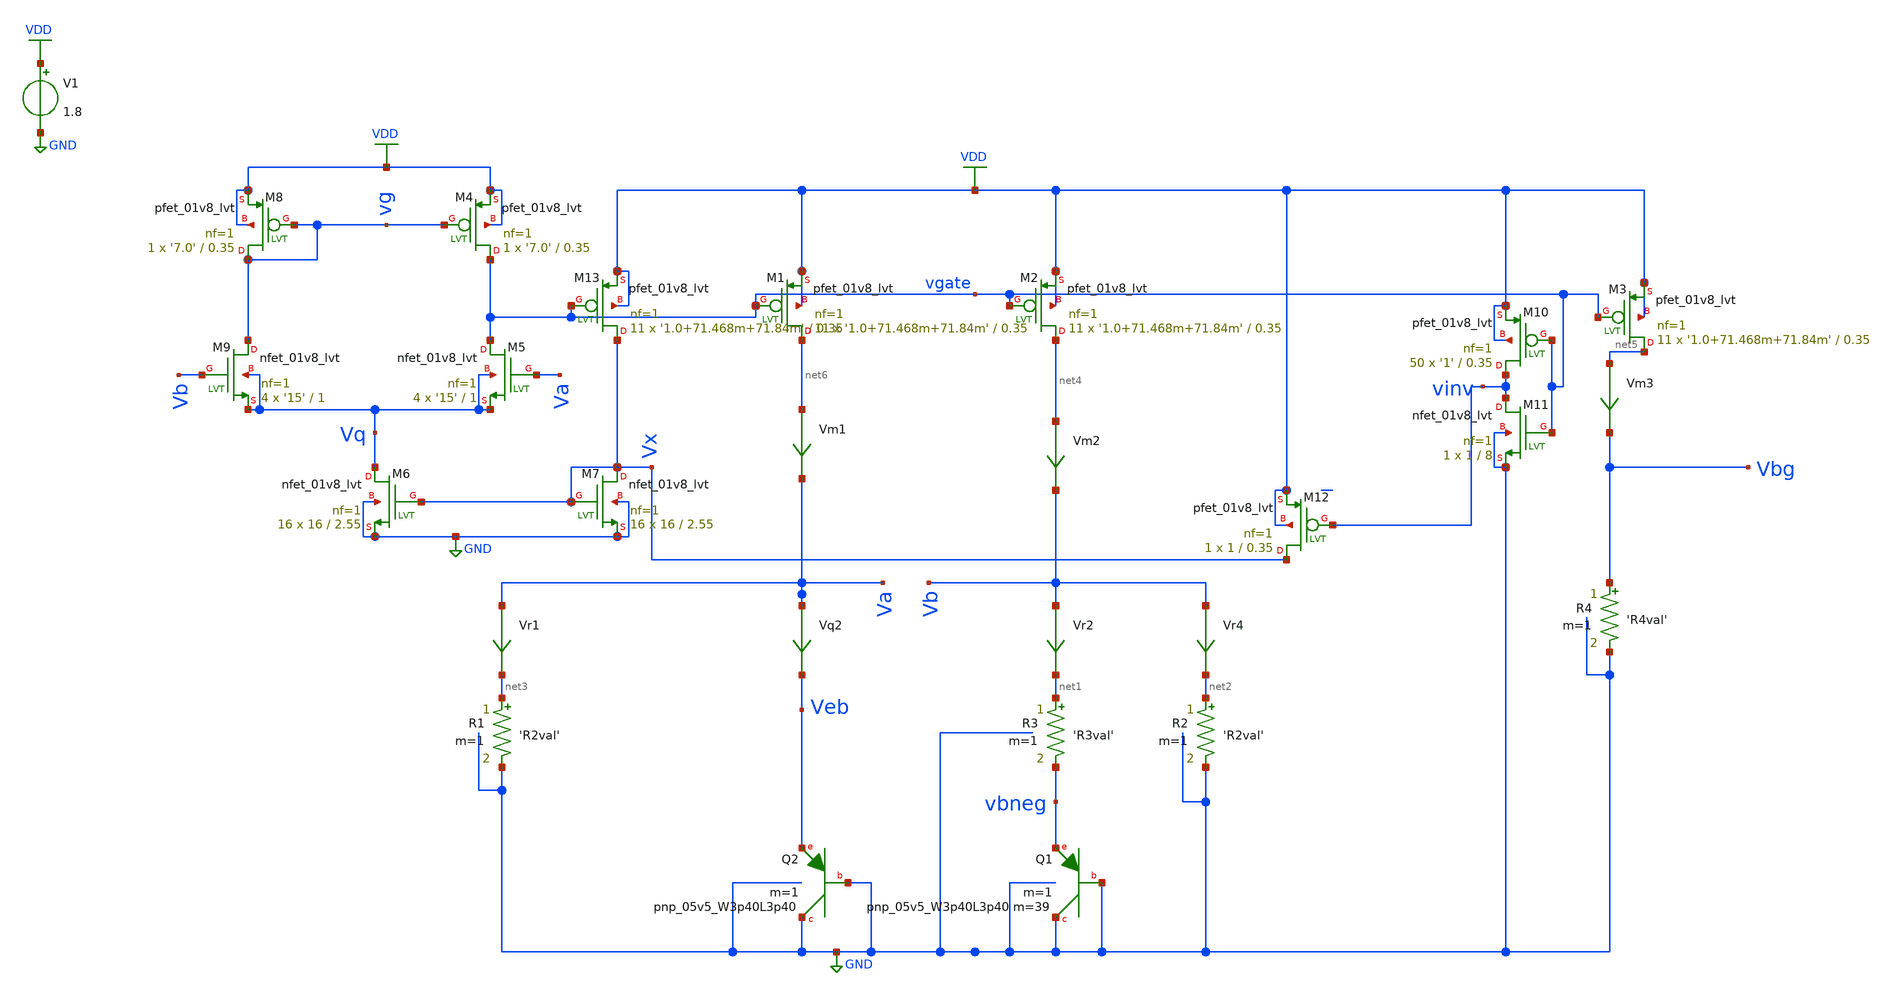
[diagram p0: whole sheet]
** sch_path: schematics/tsmc_bandgap_real_non_pdk_res.sch
**.subckt tsmc_bandgap_real_non_pdk_res
XQ2 GND GND Veb sky130_fd_pr__pnp_05v5_W3p40L3p40 m=1
V1 VDD GND 1.8
Vr4 Vb net2 0
.save i(vr4)
Vr2 Vb net1 0
.save i(vr2)
Vm1 net6 Va 0
.save i(vm1)
Vm2 net4 Vb 0
.save i(vm2)
Vm3 net5 Vbg 0
.save i(vm3)
Vr1 Va net3 0
.save i(vr1)
Vq2 Va Veb 0
.save i(vq2)
XQ1 GND GND vbneg sky130_fd_pr__pnp_05v5_W3p40L3p40 m=39 m=1
R3 net1 vbneg 'R3val' m=1
R4 Vbg GND 'R4val' m=1
R1 net3 GND 'R2val' m=1
R2 net2 GND 'R2val' m=1
XM4 vgate vg VDD VDD sky130_fd_pr__pfet_01v8_lvt L=0.35 W='7.0' nf=1 ad='int((nf+1)/2) * W/nf * 0.29'
+ as='int((nf+2)/2) * W/nf * 0.29' pd='2*int((nf+1)/2) * (W/nf + 0.29)' ps='2*int((nf+2)/2) * (W/nf + 0.29)'
+ nrd='0.29 / W' nrs='0.29 / W' sa=0 sb=0 sd=0 mult=1 m=1
XM5 vgate Va Vq Vq sky130_fd_pr__nfet_01v8_lvt L=1 W='15' nf=1 ad='int((nf+1)/2) * W/nf * 0.29' as='int((nf+2)/2) * W/nf * 0.29'
+ pd='2*int((nf+1)/2) * (W/nf + 0.29)' ps='2*int((nf+2)/2) * (W/nf + 0.29)' nrd='0.29 / W' nrs='0.29 / W'
+ sa=0 sb=0 sd=0 mult=4 m=4
XM6 Vq Vx GND GND sky130_fd_pr__nfet_01v8_lvt L=2.55 W=16 nf=1 ad='int((nf+1)/2) * W/nf * 0.29' as='int((nf+2)/2) * W/nf * 0.29'
+ pd='2*int((nf+1)/2) * (W/nf + 0.29)' ps='2*int((nf+2)/2) * (W/nf + 0.29)' nrd='0.29 / W' nrs='0.29 / W'
+ sa=0 sb=0 sd=0 mult=16 m=16
XM8 vg vg VDD VDD sky130_fd_pr__pfet_01v8_lvt L=0.35 W='7.0' nf=1 ad='int((nf+1)/2) * W/nf * 0.29' as='int((nf+2)/2) * W/nf * 0.29'
+ pd='2*int((nf+1)/2) * (W/nf + 0.29)' ps='2*int((nf+2)/2) * (W/nf + 0.29)' nrd='0.29 / W' nrs='0.29 / W'
+ sa=0 sb=0 sd=0 mult=1 m=1
XM9 vg Vb Vq Vq sky130_fd_pr__nfet_01v8_lvt L=1 W='15' nf=1 ad='int((nf+1)/2) * W/nf * 0.29' as='int((nf+2)/2) * W/nf * 0.29'
+ pd='2*int((nf+1)/2) * (W/nf + 0.29)' ps='2*int((nf+2)/2) * (W/nf + 0.29)' nrd='0.29 / W' nrs='0.29 / W'
+ sa=0 sb=0 sd=0 mult=4 m=4
XM10 vinv vgate VDD VDD sky130_fd_pr__pfet_01v8_lvt L=0.35 W='1' nf=1 ad='int((nf+1)/2) * W/nf * 0.29'
+ as='int((nf+2)/2) * W/nf * 0.29' pd='2*int((nf+1)/2) * (W/nf + 0.29)' ps='2*int((nf+2)/2) * (W/nf + 0.29)'
+ nrd='0.29 / W' nrs='0.29 / W' sa=0 sb=0 sd=0 mult=50 m=50
XM11 vinv vgate GND GND sky130_fd_pr__nfet_01v8_lvt L=8 W=1 nf=1 ad='int((nf+1)/2) * W/nf * 0.29' as='int((nf+2)/2) * W/nf * 0.29'
+ pd='2*int((nf+1)/2) * (W/nf + 0.29)' ps='2*int((nf+2)/2) * (W/nf + 0.29)' nrd='0.29 / W' nrs='0.29 / W'
+ sa=0 sb=0 sd=0 mult=1 m=1
XM12 Vx vinv VDD VDD sky130_fd_pr__pfet_01v8_lvt L=0.35 W=1 nf=1 ad='int((nf+1)/2) * W/nf * 0.29' as='int((nf+2)/2) * W/nf * 0.29'
+ pd='2*int((nf+1)/2) * (W/nf + 0.29)' ps='2*int((nf+2)/2) * (W/nf + 0.29)' nrd='0.29 / W' nrs='0.29 / W'
+ sa=0 sb=0 sd=0 mult=1 m=1
XM7 Vx Vx GND GND sky130_fd_pr__nfet_01v8_lvt L=2.55 W=16 nf=1 ad='int((nf+1)/2) * W/nf * 0.29' as='int((nf+2)/2) * W/nf * 0.29'
+ pd='2*int((nf+1)/2) * (W/nf + 0.29)' ps='2*int((nf+2)/2) * (W/nf + 0.29)' nrd='0.29 / W' nrs='0.29 / W'
+ sa=0 sb=0 sd=0 mult=16 m=16
XM13 Vx vgate VDD VDD sky130_fd_pr__pfet_01v8_lvt L=0.35 W='1.0+71.468m+71.84m' nf=1 ad='int((nf+1)/2) * W/nf * 0.29'
+ as='int((nf+2)/2) * W/nf * 0.29' pd='2*int((nf+1)/2) * (W/nf + 0.29)' ps='2*int((nf+2)/2) * (W/nf + 0.29)'
+ nrd='0.29 / W' nrs='0.29 / W' sa=0 sb=0 sd=0 mult=11 m=11
XM1 net6 vgate VDD VDD sky130_fd_pr__pfet_01v8_lvt L=0.35 W='1.0+71.468m+71.84m' nf=1 ad='int((nf+1)/2) * W/nf * 0.29'
+ as='int((nf+2)/2) * W/nf * 0.29' pd='2*int((nf+1)/2) * (W/nf + 0.29)' ps='2*int((nf+2)/2) * (W/nf + 0.29)'
+ nrd='0.29 / W' nrs='0.29 / W' sa=0 sb=0 sd=0 mult=11 m=11
XM2 net4 vgate VDD VDD sky130_fd_pr__pfet_01v8_lvt L=0.35 W='1.0+71.468m+71.84m' nf=1 ad='int((nf+1)/2) * W/nf * 0.29'
+ as='int((nf+2)/2) * W/nf * 0.29' pd='2*int((nf+1)/2) * (W/nf + 0.29)' ps='2*int((nf+2)/2) * (W/nf + 0.29)'
+ nrd='0.29 / W' nrs='0.29 / W' sa=0 sb=0 sd=0 mult=11 m=11
XM3 net5 vgate VDD VDD sky130_fd_pr__pfet_01v8_lvt L=0.35 W='1.0+71.468m+71.84m' nf=1 ad='int((nf+1)/2) * W/nf * 0.29'
+ as='int((nf+2)/2) * W/nf * 0.29' pd='2*int((nf+1)/2) * (W/nf + 0.29)' ps='2*int((nf+2)/2) * (W/nf + 0.29)'
+ nrd='0.29 / W' nrs='0.29 / W' sa=0 sb=0 sd=0 mult=11 m=11
**** begin user architecture code

.include $::SKYWATER_MODELS/cells/nfet_01v8/sky130_fd_pr__nfet_01v8__tt.corner.spice
.include $::SKYWATER_MODELS/cells/nfet_01v8_lvt/sky130_fd_pr__nfet_01v8_lvt__tt.corner.spice
.include $::SKYWATER_MODELS/cells/pfet_01v8/sky130_fd_pr__pfet_01v8__tt.corner.spice
.include $::SKYWATER_MODELS/cells/nfet_03v3_nvt/sky130_fd_pr__nfet_03v3_nvt__tt.corner.spice
.include $::SKYWATER_MODELS/cells/nfet_05v0_nvt/sky130_fd_pr__nfet_05v0_nvt__tt.corner.spice
.include $::SKYWATER_MODELS/cells/esd_nfet_01v8/sky130_fd_pr__esd_nfet_01v8__tt.corner.spice
.include $::SKYWATER_MODELS/cells/pfet_01v8_lvt/sky130_fd_pr__pfet_01v8_lvt__tt.corner.spice
.include $::SKYWATER_MODELS/cells/pfet_01v8_hvt/sky130_fd_pr__pfet_01v8_hvt__tt.corner.spice
.include $::SKYWATER_MODELS/cells/esd_pfet_g5v0d10v5/sky130_fd_pr__esd_pfet_g5v0d10v5__tt.corner.spice
.include $::SKYWATER_MODELS/cells/pfet_g5v0d10v5/sky130_fd_pr__pfet_g5v0d10v5__tt.corner.spice
.include $::SKYWATER_MODELS/cells/pfet_g5v0d16v0/sky130_fd_pr__pfet_g5v0d16v0__tt.corner.spice
.include $::SKYWATER_MODELS/cells/nfet_g5v0d10v5/sky130_fd_pr__nfet_g5v0d10v5__tt.corner.spice
.include $::SKYWATER_MODELS/cells/nfet_g5v0d16v0/sky130_fd_pr__nfet_g5v0d16v0__tt_discrete.corner.spice
.include $::SKYWATER_MODELS/cells/esd_nfet_g5v0d10v5/sky130_fd_pr__esd_nfet_g5v0d10v5__tt.corner.spice
.include $::SKYWATER_MODELS/models/corners/tt/nonfet.spice
* Mismatch parameters
.include $::SKYWATER_MODELS/cells/nfet_01v8/sky130_fd_pr__nfet_01v8__mismatch.corner.spice
.include $::SKYWATER_MODELS/cells/pfet_01v8/sky130_fd_pr__pfet_01v8__mismatch.corner.spice
.include $::SKYWATER_MODELS/cells/nfet_01v8_lvt/sky130_fd_pr__nfet_01v8_lvt__mismatch.corner.spice
.include $::SKYWATER_MODELS/cells/pfet_01v8_lvt/sky130_fd_pr__pfet_01v8_lvt__mismatch.corner.spice
.include $::SKYWATER_MODELS/cells/pfet_01v8_hvt/sky130_fd_pr__pfet_01v8_hvt__mismatch.corner.spice
.include $::SKYWATER_MODELS/cells/nfet_g5v0d10v5/sky130_fd_pr__nfet_g5v0d10v5__mismatch.corner.spice
.include $::SKYWATER_MODELS/cells/pfet_g5v0d10v5/sky130_fd_pr__pfet_g5v0d10v5__mismatch.corner.spice
.include $::SKYWATER_MODELS/cells/nfet_05v0_nvt/sky130_fd_pr__nfet_05v0_nvt__mismatch.corner.spice
.include $::SKYWATER_MODELS/cells/nfet_03v3_nvt/sky130_fd_pr__nfet_03v3_nvt__mismatch.corner.spice
* Resistor$::SKYWATER_MODELS/Capacitor
.include $::SKYWATER_MODELS/models/r+c/res_typical__cap_typical.spice
.include $::SKYWATER_MODELS/models/r+c/res_typical__cap_typical__lin.spice
* Special cells
.include $::SKYWATER_MODELS/models/corners/tt/specialized_cells.spice
* All models
.include $::SKYWATER_MODELS/models/all.spice
.include $::SKYWATER_MODELS/cells/pnp_05v5/sky130_fd_pr__pnp_05v5_W3p40L3p40.model.spice
* Corner
.include $::SKYWATER_MODELS/models/corners/tt/rf.spice



.option savecurrents
.option warn=1
.param R3val='20k/17'
.param alpha='1'
.param R2R3ratio='4.663181043*alpha'
.param R2val='R3val*R2R3ratio'
.param R4R2ratio=0.47924034354
.param R4val='R2val*R4R2ratio'
.control
save all
dc TEMP -40 140 1
plot Vbg
plot deriv(Vbg)
let i = vm3#branch
let indx = 67
*indx is the index of temperature sweep for 27degC
echo 'Vbg @ 27degC'
let vbg27c = vbg[indx]
print vbg27c
echo 'dVbe/degC & ppm @ 27degC'
print deriv(vbg)[indx] deriv(vbg)[indx]/vbg27c
plot deriv(vbg)/vbg27c
plot v(va, vb) vs i
plot vm1#branch vm2#branch vm3#branch
let vsg = vdd - vgate
let vsd1 = vdd - va
let vsd2 = vdd - vb
let vsd3 = vdd - vbg
let vthp = @m.xm1.msky130_fd_pr__pfet_01v8_lvt['vth']
let vov = vsg - vthp
plot vov vsd1 vsd2 vsd3
let deltav = vb - vbneg
let r4 =vbg/@r4[i]
let r1 =va/@r1[i]
let r2 =vb/@r2[i]
let r3 =deltav/@r3[i]
let vptat =(r2/r3*deltav)
let sum = veb+vptat
plot veb vptat sum
plot deriv(veb) deriv(vptat)
let TCratio=deriv(veb)/deriv(vptat)
plot TCratio
plot vb - va
echo 'alpha correction factor'
let alpha=TCratio[indx]
print alpha
let gm1=@m.xm1.msky130_fd_pr__pfet_01v8_lvt[gm]
let gm2=@m.xm2.msky130_fd_pr__pfet_01v8_lvt[gm]
let Av2=gm2 * ((r3 + r3/ln(39)) * r2 / (r3 + r3/ln(39) + r2) )
let Av1=gm1 * (r1 * r3/ln(39))/(r1 + r3/ln(39))
plot Av1 Av2 Av2/Av1
*write tsmc_bandgap_temp.raw
*op
*write tsmc_bandgap_op.raw
*print vbg
*print (vb - vbneg)
.endc


**** end user architecture code
**.ends
.GLOBAL GND
.GLOBAL VDD
.end
